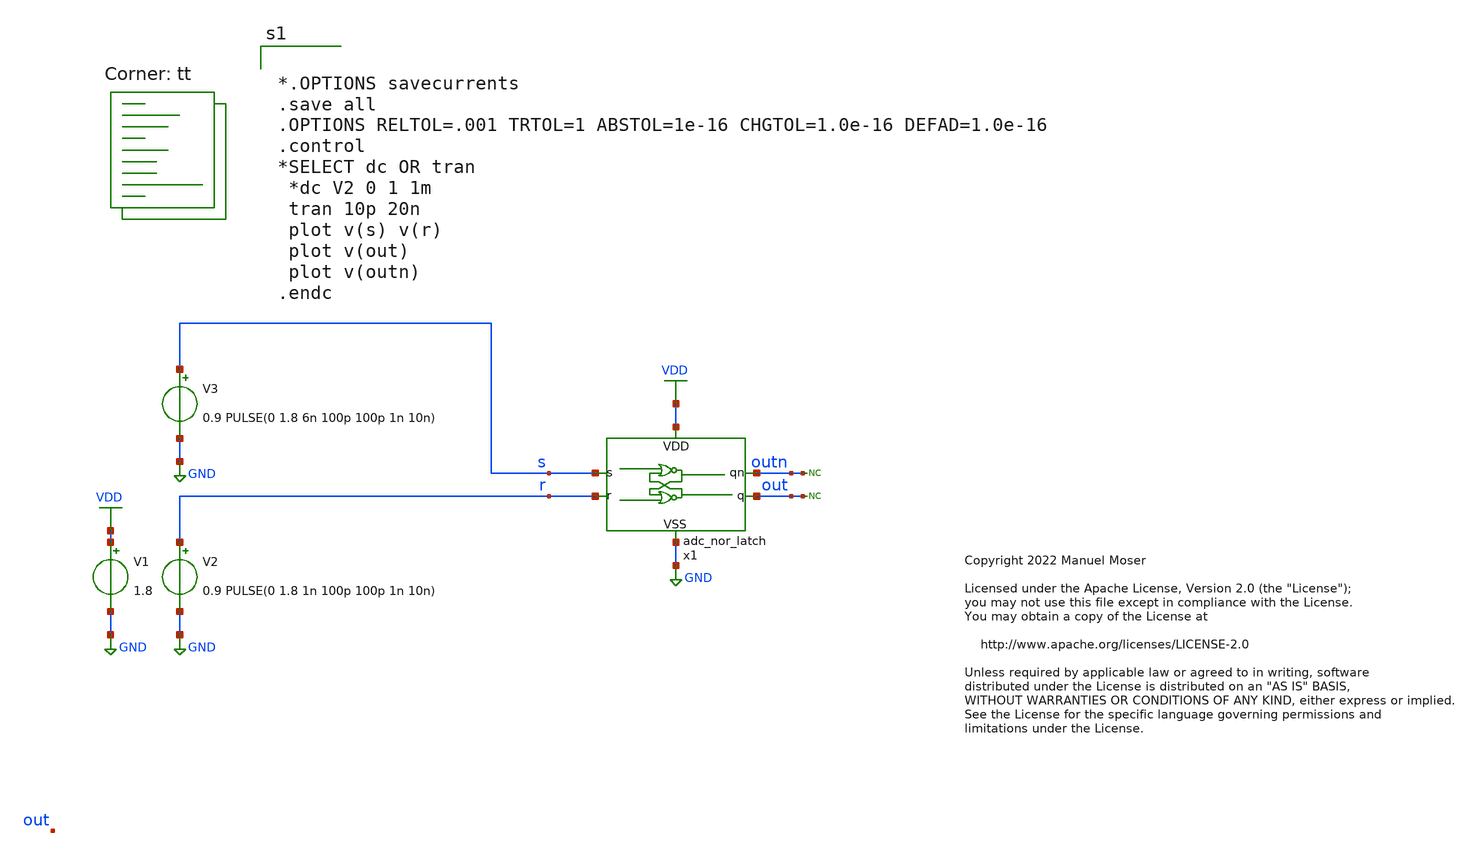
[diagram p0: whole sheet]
** sch_path: xschem/adc_nor_latch_tb.sch
* Copyright 2022 Manuel Moser
* Licensed under the Apache License, Version 2.0 (the "License");
**.subckt adc_nor_latch_tb
V1 VDD GND 1.8
V3 s GND 0.9 PULSE(0 1.8 6n 100p 100p 1n 10n)
V2 r GND 0.9 PULSE(0 1.8 1n 100p 100p 1n 10n)
* noconn out
* noconn outn
x1 s outn VDD out GND r adc_nor_latch
**** begin user architecture code


*.OPTIONS savecurrents
.save all
.OPTIONS RELTOL=.001 TRTOL=1 ABSTOL=1e-16 CHGTOL=1.0e-16 DEFAD=1.0e-16
.control
*SELECT dc OR tran
 *dc V2 0 1 1m
 tran 10p 20n
 plot v(s) v(r)
 plot v(out)
 plot v(outn)
.endc


.lib $::SKYWATER_MODELS/sky130.lib.spice tt
**** end user architecture code
**.ends

* expanding   symbol:  adc_nor_latch.sym # of pins=6
** sym_path: xschem/adc_nor_latch.sym
** sch_path: xschem/adc_nor_latch.sch
.subckt adc_nor_latch s qn VDD q VSS r
*.iopin VDD
*.iopin VSS
*.ipin s
*.ipin r
*.opin q
*.opin qn
x1 q s VDD qn VSS adc_nor
x2 qn r VDD q VSS adc_nor
.ends


* expanding   symbol:  adc_nor.sym # of pins=5
** sym_path: xschem/adc_nor.sym
** sch_path: xschem/adc_nor.sch
.subckt adc_nor b a VDD q VSS
*.iopin VDD
*.iopin VSS
*.ipin b
*.ipin a
*.opin q
XM5 q b VSS VSS sky130_fd_pr__nfet_01v8 L=0.15 W=0.42 nf=1 ad='int((nf+1)/2) * W/nf * 0.29' as='int((nf+2)/2) * W/nf * 0.29'
+ pd='2*int((nf+1)/2) * (W/nf + 0.29)' ps='2*int((nf+2)/2) * (W/nf + 0.29)' nrd='0.29 / W' nrs='0.29 / W'
+ sa=0 sb=0 sd=0 mult=1 m=1
XM6 q a VSS VSS sky130_fd_pr__nfet_01v8 L=0.15 W=0.42 nf=1 ad='int((nf+1)/2) * W/nf * 0.29' as='int((nf+2)/2) * W/nf * 0.29'
+ pd='2*int((nf+1)/2) * (W/nf + 0.29)' ps='2*int((nf+2)/2) * (W/nf + 0.29)' nrd='0.29 / W' nrs='0.29 / W'
+ sa=0 sb=0 sd=0 mult=1 m=1
XM1 q b net1 VDD sky130_fd_pr__pfet_01v8 L=0.15 W=0.8 nf=1 ad='int((nf+1)/2) * W/nf * 0.29' as='int((nf+2)/2) * W/nf * 0.29'
+ pd='2*int((nf+1)/2) * (W/nf + 0.29)' ps='2*int((nf+2)/2) * (W/nf + 0.29)' nrd='0.29 / W' nrs='0.29 / W'
+ sa=0 sb=0 sd=0 mult=1 m=1
XM2 q a net2 VDD sky130_fd_pr__pfet_01v8 L=0.15 W=0.8 nf=1 ad='int((nf+1)/2) * W/nf * 0.29' as='int((nf+2)/2) * W/nf * 0.29'
+ pd='2*int((nf+1)/2) * (W/nf + 0.29)' ps='2*int((nf+2)/2) * (W/nf + 0.29)' nrd='0.29 / W' nrs='0.29 / W'
+ sa=0 sb=0 sd=0 mult=1 m=1
XM3 net2 b VDD VDD sky130_fd_pr__pfet_01v8 L=0.15 W=0.8 nf=1 ad='int((nf+1)/2) * W/nf * 0.29' as='int((nf+2)/2) * W/nf * 0.29'
+ pd='2*int((nf+1)/2) * (W/nf + 0.29)' ps='2*int((nf+2)/2) * (W/nf + 0.29)' nrd='0.29 / W' nrs='0.29 / W'
+ sa=0 sb=0 sd=0 mult=1 m=1
XM4 net1 a VDD VDD sky130_fd_pr__pfet_01v8 L=0.15 W=0.8 nf=1 ad='int((nf+1)/2) * W/nf * 0.29' as='int((nf+2)/2) * W/nf * 0.29'
+ pd='2*int((nf+1)/2) * (W/nf + 0.29)' ps='2*int((nf+2)/2) * (W/nf + 0.29)' nrd='0.29 / W' nrs='0.29 / W'
+ sa=0 sb=0 sd=0 mult=1 m=1
.ends

.GLOBAL GND
.GLOBAL VDD
.end
